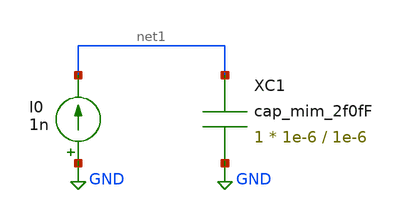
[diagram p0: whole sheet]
** sch_path: Clock_Reference/clockGenerator/clockGenerator/untitled.sch
**.subckt untitled
XC1 net1 GND cap_mim_2f0fF c_width=1e-6 c_length=1e-6 m=1
I0 GND net1 1n
**.ends
.GLOBAL GND
.end
